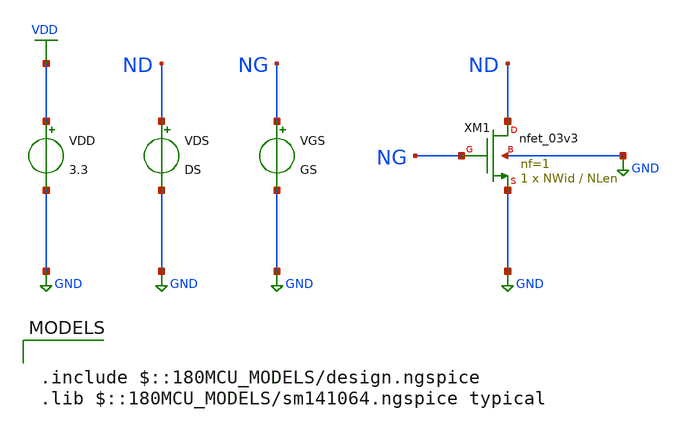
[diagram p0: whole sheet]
** sch_path: Design_Files/IC Design/Testbench/SIZING/Gm_Id/NMOS_Gm_Id.sch
**.subckt NMOS_Gm_Id
XM1 ND NG GND GND nfet_03v3 L=NLen W=NWid nf=1 ad='int((nf+1)/2) * W/nf * 0.18u' as='int((nf+2)/2) * W/nf * 0.18u'
+ pd='2*int((nf+1)/2) * (W/nf + 0.18u)' ps='2*int((nf+2)/2) * (W/nf + 0.18u)' nrd='0.18u / W' nrs='0.18u / W'
+ sa=0 sb=0 sd=0 m=1
VGS NG GND GS
.save i(vgs)
VDS ND GND DS
.save i(vds)
VDD VDD GND 3.3
**** begin user architecture code



.param NWid=10u
.param NLen=1u
.param GS=0
.param DS=1.65

.control

shell mkdir -p
+ /foss/designs/ECG_Acquisition_IC/Measurement_Results/IC_Simulation/SIZING/Gm_Id/NMOS_Gm_Id/Results_txt

set wr_vecnames
set wr_singlescale

* =========================================================
* NMOS gm/Id + fT 2D DC sweep
* W fixed at 10u
* VGS: 0 to 3.3 V
* VDS: 0 to 3.3 V
* Export: VGS VDS ID ID/W gm gds Cgs Cgd Cgb Cgg fT
* =========================================================

alterparam NLen = 0.28u
reset
save v(ng) v(nd) vds#branch @m.xm1.m0[gm] @m.xm1.m0[gds] @m.xm1.m0[cgs] @m.xm1.m0[cgd]
+ @m.xm1.m0[cgb]
dc VGS 0 3.3 0.01 VDS 0 3.3 0.05
let vgs_out = v(ng)
let vds_out = v(nd)
let id = abs(vds#branch)
let id_w = id/10e-6
let gm = abs(@m.xm1.m0[gm])
let gds = abs(@m.xm1.m0[gds])
let cgs = abs(@m.xm1.m0[cgs])
let cgd = abs(@m.xm1.m0[cgd])
let cgb = abs(@m.xm1.m0[cgb])
let cgg = cgs + cgd + cgb
let ft_hz = gm/(6.283185307179586*(cgg + 1e-30))
let ft_mhz = ft_hz/1e6
wrdata
+ /foss/designs/ECG_Acquisition_IC/Measurement_Results/IC_Simulation/SIZING/Gm_Id/NMOS_Gm_Id/Results_txt/nmos_L0p28u_W10u.txt vgs_out vds_out id id_w gm gds cgs cgd cgb cgg ft_hz ft_mhz

alterparam NLen = 0.5u
reset
save v(ng) v(nd) vds#branch @m.xm1.m0[gm] @m.xm1.m0[gds] @m.xm1.m0[cgs] @m.xm1.m0[cgd]
+ @m.xm1.m0[cgb]
dc VGS 0 3.3 0.01 VDS 0 3.3 0.05
let vgs_out = v(ng)
let vds_out = v(nd)
let id = abs(vds#branch)
let id_w = id/10e-6
let gm = abs(@m.xm1.m0[gm])
let gds = abs(@m.xm1.m0[gds])
let cgs = abs(@m.xm1.m0[cgs])
let cgd = abs(@m.xm1.m0[cgd])
let cgb = abs(@m.xm1.m0[cgb])
let cgg = cgs + cgd + cgb
let ft_hz = gm/(6.283185307179586*(cgg + 1e-30))
let ft_mhz = ft_hz/1e6
wrdata
+ /foss/designs/ECG_Acquisition_IC/Measurement_Results/IC_Simulation/SIZING/Gm_Id/NMOS_Gm_Id/Results_txt/nmos_L0p5u_W10u.txt vgs_out vds_out id id_w gm gds cgs cgd cgb cgg ft_hz ft_mhz

alterparam NLen = 1u
reset
save v(ng) v(nd) vds#branch @m.xm1.m0[gm] @m.xm1.m0[gds] @m.xm1.m0[cgs] @m.xm1.m0[cgd]
+ @m.xm1.m0[cgb]
dc VGS 0 3.3 0.01 VDS 0 3.3 0.05
let vgs_out = v(ng)
let vds_out = v(nd)
let id = abs(vds#branch)
let id_w = id/10e-6
let gm = abs(@m.xm1.m0[gm])
let gds = abs(@m.xm1.m0[gds])
let cgs = abs(@m.xm1.m0[cgs])
let cgd = abs(@m.xm1.m0[cgd])
let cgb = abs(@m.xm1.m0[cgb])
let cgg = cgs + cgd + cgb
let ft_hz = gm/(6.283185307179586*(cgg + 1e-30))
let ft_mhz = ft_hz/1e6
wrdata
+ /foss/designs/ECG_Acquisition_IC/Measurement_Results/IC_Simulation/SIZING/Gm_Id/NMOS_Gm_Id/Results_txt/nmos_L1u_W10u.txt vgs_out vds_out id id_w gm gds cgs cgd cgb cgg ft_hz ft_mhz

alterparam NLen = 1.5u
reset
save v(ng) v(nd) vds#branch @m.xm1.m0[gm] @m.xm1.m0[gds] @m.xm1.m0[cgs] @m.xm1.m0[cgd]
+ @m.xm1.m0[cgb]
dc VGS 0 3.3 0.01 VDS 0 3.3 0.05
let vgs_out = v(ng)
let vds_out = v(nd)
let id = abs(vds#branch)
let id_w = id/10e-6
let gm = abs(@m.xm1.m0[gm])
let gds = abs(@m.xm1.m0[gds])
let cgs = abs(@m.xm1.m0[cgs])
let cgd = abs(@m.xm1.m0[cgd])
let cgb = abs(@m.xm1.m0[cgb])
let cgg = cgs + cgd + cgb
let ft_hz = gm/(6.283185307179586*(cgg + 1e-30))
let ft_mhz = ft_hz/1e6
wrdata
+ /foss/designs/ECG_Acquisition_IC/Measurement_Results/IC_Simulation/SIZING/Gm_Id/NMOS_Gm_Id/Results_txt/nmos_L1p5u_W10u.txt vgs_out vds_out id id_w gm gds cgs cgd cgb cgg ft_hz ft_mhz

alterparam NLen = 2u
reset
save v(ng) v(nd) vds#branch @m.xm1.m0[gm] @m.xm1.m0[gds] @m.xm1.m0[cgs] @m.xm1.m0[cgd]
+ @m.xm1.m0[cgb]
dc VGS 0 3.3 0.01 VDS 0 3.3 0.05
let vgs_out = v(ng)
let vds_out = v(nd)
let id = abs(vds#branch)
let id_w = id/10e-6
let gm = abs(@m.xm1.m0[gm])
let gds = abs(@m.xm1.m0[gds])
let cgs = abs(@m.xm1.m0[cgs])
let cgd = abs(@m.xm1.m0[cgd])
let cgb = abs(@m.xm1.m0[cgb])
let cgg = cgs + cgd + cgb
let ft_hz = gm/(6.283185307179586*(cgg + 1e-30))
let ft_mhz = ft_hz/1e6
wrdata
+ /foss/designs/ECG_Acquisition_IC/Measurement_Results/IC_Simulation/SIZING/Gm_Id/NMOS_Gm_Id/Results_txt/nmos_L2u_W10u.txt vgs_out vds_out id id_w gm gds cgs cgd cgb cgg ft_hz ft_mhz

alterparam NLen = 3u
reset
save v(ng) v(nd) vds#branch @m.xm1.m0[gm] @m.xm1.m0[gds] @m.xm1.m0[cgs] @m.xm1.m0[cgd]
+ @m.xm1.m0[cgb]
dc VGS 0 3.3 0.01 VDS 0 3.3 0.05
let vgs_out = v(ng)
let vds_out = v(nd)
let id = abs(vds#branch)
let id_w = id/10e-6
let gm = abs(@m.xm1.m0[gm])
let gds = abs(@m.xm1.m0[gds])
let cgs = abs(@m.xm1.m0[cgs])
let cgd = abs(@m.xm1.m0[cgd])
let cgb = abs(@m.xm1.m0[cgb])
let cgg = cgs + cgd + cgb
let ft_hz = gm/(6.283185307179586*(cgg + 1e-30))
let ft_mhz = ft_hz/1e6
wrdata
+ /foss/designs/ECG_Acquisition_IC/Measurement_Results/IC_Simulation/SIZING/Gm_Id/NMOS_Gm_Id/Results_txt/nmos_L3u_W10u.txt vgs_out vds_out id id_w gm gds cgs cgd cgb cgg ft_hz ft_mhz

alterparam NLen = 4u
reset
save v(ng) v(nd) vds#branch @m.xm1.m0[gm] @m.xm1.m0[gds] @m.xm1.m0[cgs] @m.xm1.m0[cgd]
+ @m.xm1.m0[cgb]
dc VGS 0 3.3 0.01 VDS 0 3.3 0.05
let vgs_out = v(ng)
let vds_out = v(nd)
let id = abs(vds#branch)
let id_w = id/10e-6
let gm = abs(@m.xm1.m0[gm])
let gds = abs(@m.xm1.m0[gds])
let cgs = abs(@m.xm1.m0[cgs])
let cgd = abs(@m.xm1.m0[cgd])
let cgb = abs(@m.xm1.m0[cgb])
let cgg = cgs + cgd + cgb
let ft_hz = gm/(6.283185307179586*(cgg + 1e-30))
let ft_mhz = ft_hz/1e6
wrdata
+ /foss/designs/ECG_Acquisition_IC/Measurement_Results/IC_Simulation/SIZING/Gm_Id/NMOS_Gm_Id/Results_txt/nmos_L4u_W10u.txt vgs_out vds_out id id_w gm gds cgs cgd cgb cgg ft_hz ft_mhz

alterparam NLen = 5u
reset
save v(ng) v(nd) vds#branch @m.xm1.m0[gm] @m.xm1.m0[gds] @m.xm1.m0[cgs] @m.xm1.m0[cgd]
+ @m.xm1.m0[cgb]
dc VGS 0 3.3 0.01 VDS 0 3.3 0.05
let vgs_out = v(ng)
let vds_out = v(nd)
let id = abs(vds#branch)
let id_w = id/10e-6
let gm = abs(@m.xm1.m0[gm])
let gds = abs(@m.xm1.m0[gds])
let cgs = abs(@m.xm1.m0[cgs])
let cgd = abs(@m.xm1.m0[cgd])
let cgb = abs(@m.xm1.m0[cgb])
let cgg = cgs + cgd + cgb
let ft_hz = gm/(6.283185307179586*(cgg + 1e-30))
let ft_mhz = ft_hz/1e6
wrdata
+ /foss/designs/ECG_Acquisition_IC/Measurement_Results/IC_Simulation/SIZING/Gm_Id/NMOS_Gm_Id/Results_txt/nmos_L5u_W10u.txt vgs_out vds_out id id_w gm gds cgs cgd cgb cgg ft_hz ft_mhz

.endc



.include $::180MCU_MODELS/design.ngspice
.lib $::180MCU_MODELS/sm141064.ngspice typical

**** end user architecture code
**.ends
.GLOBAL GND
.GLOBAL VDD
.end
